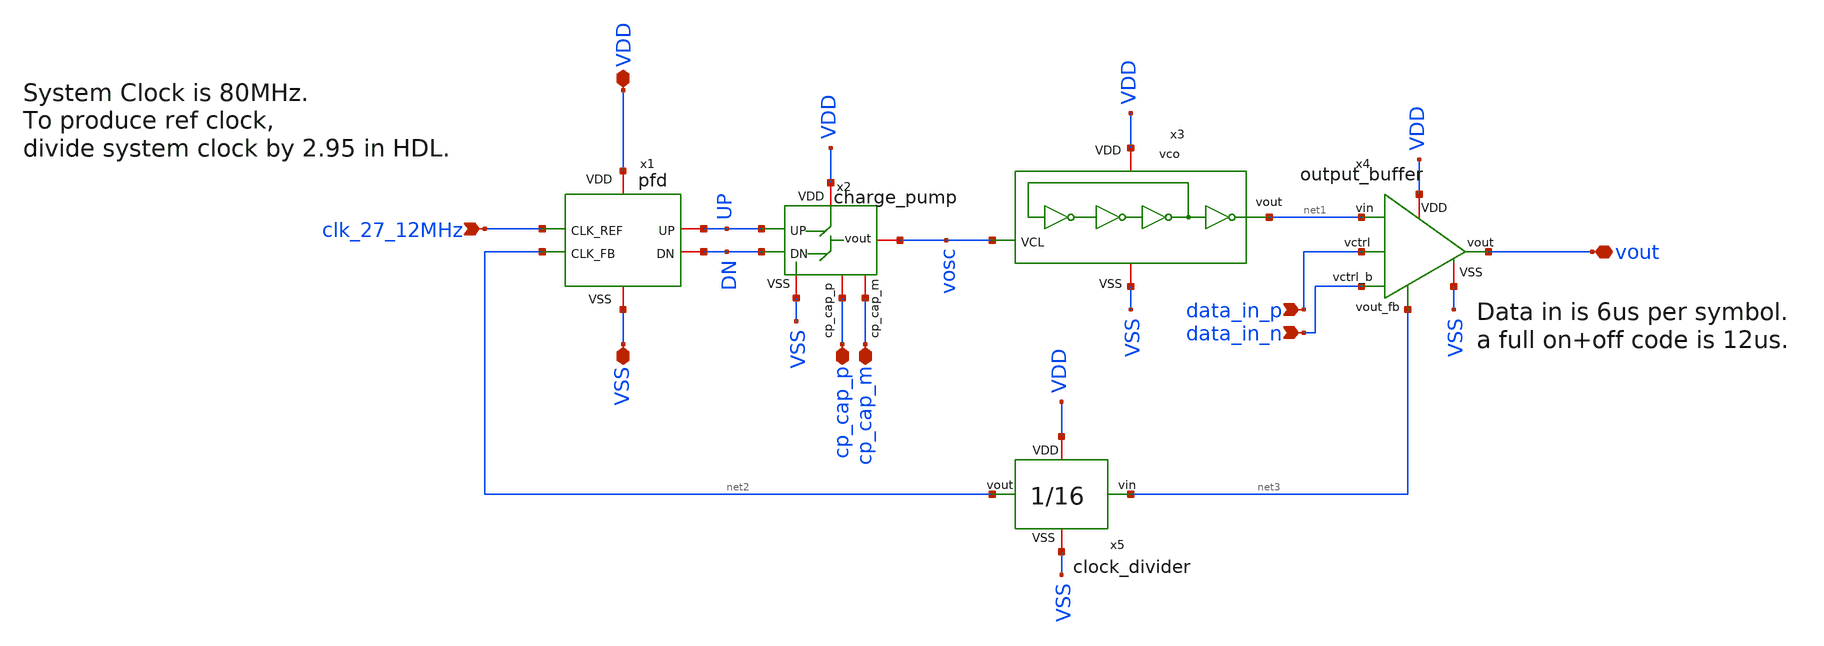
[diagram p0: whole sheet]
** sch_path: macros/heichips26_ook/macros/ook_analog_system/schematic/xschem/ook_transmitter.sch
**.subckt ook_transmitter VDD VSS data_in_n clk_27_12MHz vout data_in_p cp_cap_p cp_cap_m
*.iopin VDD
*.iopin VSS
*.ipin data_in_n
*.ipin clk_27_12MHz
*.iopin vout
*.ipin data_in_p
*.iopin cp_cap_p
*.iopin cp_cap_m
x1 clk_27_12MHz UP DN net2 VDD VSS pfd
x2 cp_cap_m cp_cap_p VSS VDD UP vosc DN charge_pump
x3 net1 VDD VSS vosc vco
x4 net3 data_in_p VDD net1 vout VSS data_in_n output_buffer
x5 VDD net2 net3 VSS clock_divider
**.ends
.end
